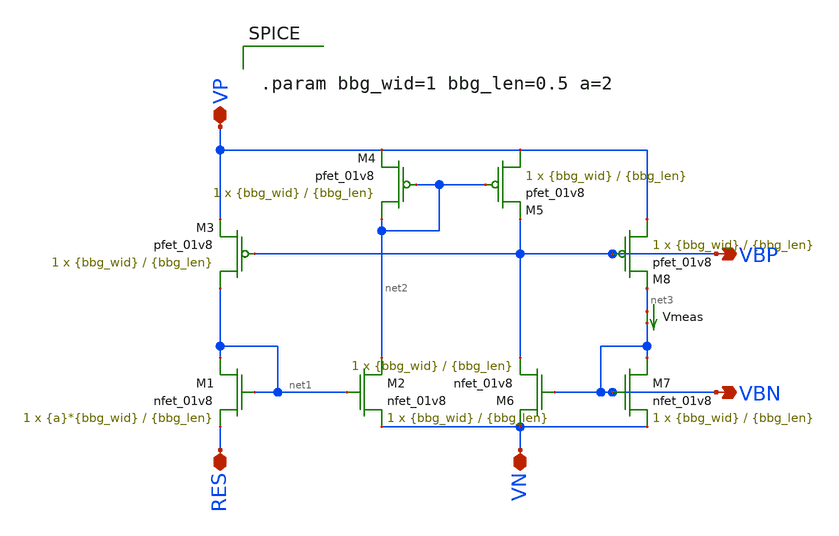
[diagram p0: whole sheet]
** sch_path: bbg.sch
**.subckt bbg VP VN RES VBP VBN
*.iopin VP
*.iopin VN
*.iopin RES
*.opin VBP
*.opin VBN
XM1 net1 net1 RES VN sky130_fd_pr__nfet_01v8 L={bbg_len} W={a}*{bbg_wid} nf=1 ad='int((nf+1)/2) * W/nf * 0.29'
+ as='int((nf+2)/2) * W/nf * 0.29' pd='2*int((nf+1)/2) * (W/nf + 0.29)' ps='2*int((nf+2)/2) * (W/nf + 0.29)'
+ nrd='0.29 / W' nrs='0.29 / W' sa=0 sb=0 sd=0 mult=1 m=1
XM2 net2 net1 VN VN sky130_fd_pr__nfet_01v8 L={bbg_len} W={bbg_wid} nf=1 ad='int((nf+1)/2) * W/nf * 0.29'
+ as='int((nf+2)/2) * W/nf * 0.29' pd='2*int((nf+1)/2) * (W/nf + 0.29)' ps='2*int((nf+2)/2) * (W/nf + 0.29)'
+ nrd='0.29 / W' nrs='0.29 / W' sa=0 sb=0 sd=0 mult=1 m=1
XM3 net1 VBP VP VP sky130_fd_pr__pfet_01v8 L={bbg_len} W={bbg_wid} nf=1 ad='int((nf+1)/2) * W/nf * 0.29'
+ as='int((nf+2)/2) * W/nf * 0.29' pd='2*int((nf+1)/2) * (W/nf + 0.29)' ps='2*int((nf+2)/2) * (W/nf + 0.29)'
+ nrd='0.29 / W' nrs='0.29 / W' sa=0 sb=0 sd=0 mult=1 m=1
Vmeas net3 VBN 0
.save i(vmeas)
XM6 VN VBN VBP VN sky130_fd_pr__nfet_01v8 L={bbg_len} W={bbg_wid} nf=1 ad='int((nf+1)/2) * W/nf * 0.29'
+ as='int((nf+2)/2) * W/nf * 0.29' pd='2*int((nf+1)/2) * (W/nf + 0.29)' ps='2*int((nf+2)/2) * (W/nf + 0.29)'
+ nrd='0.29 / W' nrs='0.29 / W' sa=0 sb=0 sd=0 mult=1 m=1
XM7 VBN VBN VN VN sky130_fd_pr__nfet_01v8 L={bbg_len} W={bbg_wid} nf=1 ad='int((nf+1)/2) * W/nf * 0.29'
+ as='int((nf+2)/2) * W/nf * 0.29' pd='2*int((nf+1)/2) * (W/nf + 0.29)' ps='2*int((nf+2)/2) * (W/nf + 0.29)'
+ nrd='0.29 / W' nrs='0.29 / W' sa=0 sb=0 sd=0 mult=1 m=1
XM4 net2 net2 VP VP sky130_fd_pr__pfet_01v8 L={bbg_len} W={bbg_wid} nf=1 ad='int((nf+1)/2) * W/nf * 0.29'
+ as='int((nf+2)/2) * W/nf * 0.29' pd='2*int((nf+1)/2) * (W/nf + 0.29)' ps='2*int((nf+2)/2) * (W/nf + 0.29)'
+ nrd='0.29 / W' nrs='0.29 / W' sa=0 sb=0 sd=0 mult=1 m=1
XM5 VP net2 VBP VP sky130_fd_pr__pfet_01v8 L={bbg_len} W={bbg_wid} nf=1 ad='int((nf+1)/2) * W/nf * 0.29'
+ as='int((nf+2)/2) * W/nf * 0.29' pd='2*int((nf+1)/2) * (W/nf + 0.29)' ps='2*int((nf+2)/2) * (W/nf + 0.29)'
+ nrd='0.29 / W' nrs='0.29 / W' sa=0 sb=0 sd=0 mult=1 m=1
XM8 VP VBP net3 VP sky130_fd_pr__pfet_01v8 L={bbg_len} W={bbg_wid} nf=1 ad='int((nf+1)/2) * W/nf * 0.29'
+ as='int((nf+2)/2) * W/nf * 0.29' pd='2*int((nf+1)/2) * (W/nf + 0.29)' ps='2*int((nf+2)/2) * (W/nf + 0.29)'
+ nrd='0.29 / W' nrs='0.29 / W' sa=0 sb=0 sd=0 mult=1 m=1
**** begin user architecture code


.param bbg_wid=1 bbg_len=0.5 a=2


**** end user architecture code
**.ends
.end
